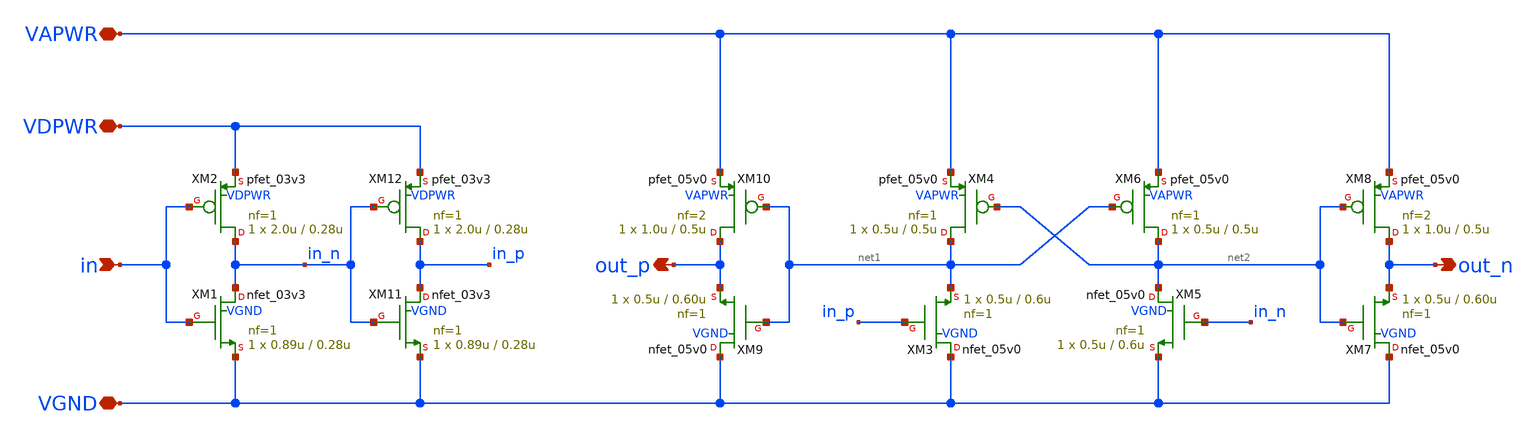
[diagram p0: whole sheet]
** sch_path: pg/gf180mcuD/tt_pg_5v0_2/xschem/lv2hv.sch
**.subckt lv2hv VAPWR VGND in VDPWR out_p out_n
*.iopin VAPWR
*.iopin VGND
*.ipin in
*.iopin VDPWR
*.opin out_p
*.opin out_n
XM1 in_n in VGND VGND nfet_03v3 L=0.28u W=0.89u nf=1 ad='int((nf+1)/2) * W/nf * 0.18u' as='int((nf+2)/2) * W/nf * 0.18u'
+ pd='2*int((nf+1)/2) * (W/nf + 0.18u)' ps='2*int((nf+2)/2) * (W/nf + 0.18u)' nrd='0.18u / W' nrs='0.18u / W'
+ sa=0 sb=0 sd=0 m=1 par=1
XM2 in_n in VDPWR VDPWR pfet_03v3 L=0.28u W=2.0u nf=1 ad='int((nf+1)/2) * W/nf * 0.18u' as='int((nf+2)/2) * W/nf * 0.18u'
+ pd='2*int((nf+1)/2) * (W/nf + 0.18u)' ps='2*int((nf+2)/2) * (W/nf + 0.18u)' nrd='0.18u / W' nrs='0.18u / W'
+ sa=0 sb=0 sd=0 m=1 par=1
XM3 VGND in_p net1 VGND nfet_05v0 L=0.6u W=0.5u nf=1 ad='int((nf+1)/2) * W/nf * 0.18u' as='int((nf+2)/2) * W/nf * 0.18u'
+ pd='2*int((nf+1)/2) * (W/nf + 0.18u)' ps='2*int((nf+2)/2) * (W/nf + 0.18u)' nrd='0.18u / W' nrs='0.18u / W'
+ sa=0 sb=0 sd=0 m=1 par=1
XM4 net1 net2 VAPWR VAPWR pfet_05v0 L=0.5u W=0.5u nf=1 ad='int((nf+1)/2) * W/nf * 0.18u' as='int((nf+2)/2) * W/nf * 0.18u'
+ pd='2*int((nf+1)/2) * (W/nf + 0.18u)' ps='2*int((nf+2)/2) * (W/nf + 0.18u)' nrd='0.18u / W' nrs='0.18u / W'
+ sa=0 sb=0 sd=0 m=1 par=1
XM5 net2 in_n VGND VGND nfet_05v0 L=0.6u W=0.5u nf=1 ad='int((nf+1)/2) * W/nf * 0.18u' as='int((nf+2)/2) * W/nf * 0.18u'
+ pd='2*int((nf+1)/2) * (W/nf + 0.18u)' ps='2*int((nf+2)/2) * (W/nf + 0.18u)' nrd='0.18u / W' nrs='0.18u / W'
+ sa=0 sb=0 sd=0 m=1 par=1
XM6 net2 net1 VAPWR VAPWR pfet_05v0 L=0.5u W=0.5u nf=1 ad='int((nf+1)/2) * W/nf * 0.18u' as='int((nf+2)/2) * W/nf * 0.18u'
+ pd='2*int((nf+1)/2) * (W/nf + 0.18u)' ps='2*int((nf+2)/2) * (W/nf + 0.18u)' nrd='0.18u / W' nrs='0.18u / W'
+ sa=0 sb=0 sd=0 m=1 par=1
XM7 VGND net2 out_n VGND nfet_05v0 L=0.60u W=0.5u nf=1 ad='int((nf+1)/2) * W/nf * 0.18u' as='int((nf+2)/2) * W/nf * 0.18u'
+ pd='2*int((nf+1)/2) * (W/nf + 0.18u)' ps='2*int((nf+2)/2) * (W/nf + 0.18u)' nrd='0.18u / W' nrs='0.18u / W'
+ sa=0 sb=0 sd=0 m=1 par=1
XM8 out_n net2 VAPWR VAPWR pfet_05v0 L=0.5u W=1.0u nf=2 ad='int((nf+1)/2) * W/nf * 0.18u' as='int((nf+2)/2) * W/nf * 0.18u'
+ pd='2*int((nf+1)/2) * (W/nf + 0.18u)' ps='2*int((nf+2)/2) * (W/nf + 0.18u)' nrd='0.18u / W' nrs='0.18u / W'
+ sa=0 sb=0 sd=0 m=1 par=1
XM9 VGND net1 out_p VGND nfet_05v0 L=0.60u W=0.5u nf=1 ad='int((nf+1)/2) * W/nf * 0.18u' as='int((nf+2)/2) * W/nf * 0.18u'
+ pd='2*int((nf+1)/2) * (W/nf + 0.18u)' ps='2*int((nf+2)/2) * (W/nf + 0.18u)' nrd='0.18u / W' nrs='0.18u / W'
+ sa=0 sb=0 sd=0 m=1 par=1
XM10 out_p net1 VAPWR VAPWR pfet_05v0 L=0.5u W=1.0u nf=2 ad='int((nf+1)/2) * W/nf * 0.18u' as='int((nf+2)/2) * W/nf * 0.18u'
+ pd='2*int((nf+1)/2) * (W/nf + 0.18u)' ps='2*int((nf+2)/2) * (W/nf + 0.18u)' nrd='0.18u / W' nrs='0.18u / W'
+ sa=0 sb=0 sd=0 m=1 par=1
XM11 in_p in_n VGND VGND nfet_03v3 L=0.28u W=0.89u nf=1 ad='int((nf+1)/2) * W/nf * 0.18u' as='int((nf+2)/2) * W/nf * 0.18u'
+ pd='2*int((nf+1)/2) * (W/nf + 0.18u)' ps='2*int((nf+2)/2) * (W/nf + 0.18u)' nrd='0.18u / W' nrs='0.18u / W'
+ sa=0 sb=0 sd=0 m=1 par=1
XM12 in_p in_n VDPWR VDPWR pfet_03v3 L=0.28u W=2.0u nf=1 ad='int((nf+1)/2) * W/nf * 0.18u' as='int((nf+2)/2) * W/nf * 0.18u'
+ pd='2*int((nf+1)/2) * (W/nf + 0.18u)' ps='2*int((nf+2)/2) * (W/nf + 0.18u)' nrd='0.18u / W' nrs='0.18u / W'
+ sa=0 sb=0 sd=0 m=1 par=1
**.ends
.end
